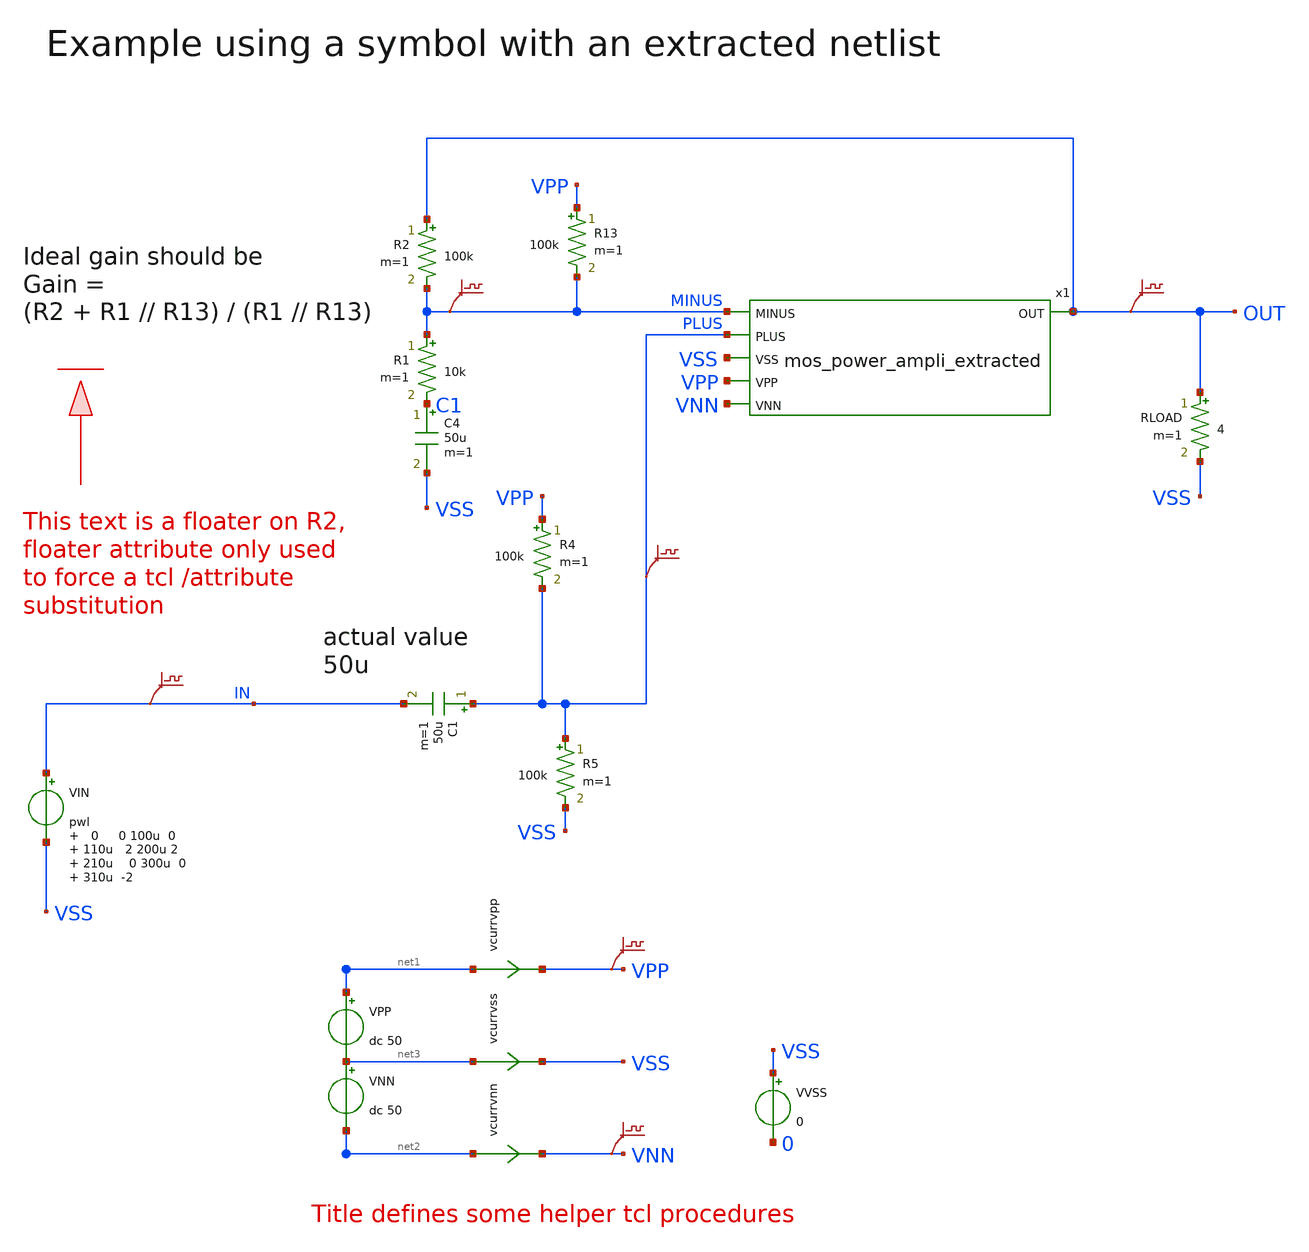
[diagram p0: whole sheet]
** sch_path: xschem-src/xschem_library/examples/test_extracted_netlist.sch
* Copyright (C) 1998-2026 Stefan Frederik Schippers
* This program is free software; you can redistribute it and/or modify
* it under the terms of the GNU General Public License as published by
* the Free Software Foundation; either version 2 of the License, or
* (at your option) any later version.
* This program is distributed in the hope that it will be useful,
* but WITHOUT ANY WARRANTY; without even the implied warranty of
* MERCHANTABILITY or FITNESS FOR A PARTICULAR PURPOSE.  See the
* GNU General Public License for more details.
* You should have received a copy of the GNU General Public License
* along with this program; if not, write to the Free Software
**.subckt test_extracted_netlist
R1 MINUS C1 10k m=1
R2 OUT MINUS 100k m=1
VPP net1 net3 dc 50
VNN net3 net2 dc 50
vcurrvpp net1 VPP 0
.save i(vcurrvpp)
vcurrvnn net2 VNN 0
.save i(vcurrvnn)
vcurrvss net3 VSS 0
.save i(vcurrvss)
.save v(vpp)
.save v(vnn)
VVSS VSS 0 0
VIN IN VSS pwl 0 0 100u 0 110u 2 200u 2 210u 0 300u 0 310u -2
.save v(out)
.save v(minus)
.save v(in)
R4 VPP PLUS 100k m=1
R5 PLUS VSS 100k m=1
C1 PLUS IN 50u m=1
C4 C1 VSS 50u m=1
R13 VPP MINUS 100k m=1
RLOAD OUT VSS 4 m=1
.save v(plus)
x1 MINUS PLUS VSS OUT VPP VNN mos_power_ampli_extracted
**** begin user architecture code

.include "models_poweramp.txt"
.options method=gear savecurrents ITL4=500 ITL5=50000  CHGTOL=1e-15 TRTOL=1
.control
save all
op
write test_extracted_netlist.raw
set appendwrite
tran  100n 400u
* .FOUR 20k v(outm,outp)
* .probe i(*)
write test_extracted_netlist.raw
.endc


**** end user architecture code
**.ends

* expanding   symbol:  mos_power_ampli_extracted.sym # of pins=6
** sym_path: xschem-src/xschem_library/examples/mos_power_ampli_extracted.sym
** sch_path: xschem-src/xschem_library/examples/mos_power_ampli_extracted.sch
.subckt mos_power_ampli_extracted MINUS PLUS VSS OUT VPP VNN
*.ipin PLUS
*.ipin VPP
*.ipin VNN
*.opin OUT
*.ipin MINUS
*.ipin VSS
* noconn MINUS
* noconn PLUS
* noconn VSS
* noconn VPP
* noconn VNN
* noconn OUT
**** begin user architecture code
xm2 net1 GB SB irf540 m=1
R7 GB SB 190 m=1
xm1 VPP GA SA irf540 m=1
R0 GA SA 190 m=1
R2 VPP E2 50 m=1
R3 VBOOST E1 50 m=1
Q5 C5 PLUS E9 q2n2222 area=1 m=1
Q4 net8 net2 E4 q2n2907p area=1 m=1
R9 VBOOST E4 50 m=1
Q6 C6 C2 net5 q2n2907p area=1 m=1
R4 VPP E6 50 m=1
vd OUTI net1 0
.save  i(vd)
vu SA OUTI 0
.save  i(vu)
Q1 net2 net2 E1 q2n2907p area=1 m=1
Q2 C2 C2 net4 q2n2907p area=1 m=1
Q9 C9 MINUS E9 q2n2222 area=1 m=1
R11 GB net6 1300 m=1
Q8 C8 VSS E8 q2n2907p area=1 m=1
C12 VBOOST net3 40u m=1
D0 VPP VBOOST d1n4148 area=1
R18 net3 OUTI 200 m=1
D1 VPP VBOOST d1n758
R14 B1 net7 4k m=1
Q11 GA B1 E11 q2n2907p area=1 m=1
R15 VBOOST B1 4k m=1
R5 E9 net9 120 m=1
R6 net9 net10 120 m=1
D2 VSS B3 d1n755
Q3 C3 B3 E3 q2n2222 area=1 m=1
R1 VPP B3 10k m=1
R10 E3 VSS 170 m=1
C3 B3 VSS 100n m=1
R12 C6 E8 1300 m=1
R13 C2 C9 300 m=1
Q7 C7 C9 C5 q2n2222 area=1 m=1
v0 SB VNN 0
.save  i(v0)
v1 E6 net5 0
.save  i(v1)
v2 E2 net4 0
.save  i(v2)
v3 net10 C3 0
.save  i(v3)
v4 C8 net6 0
.save  i(v4)
v5 net7 OUTI 0
.save  i(v5)
v6 net2 C7 0
.save  i(v6)
v7 net8 E11 0
.save  i(v7)
.save  v(gb)
.save  v(sb)
.save  v(ga)
.save  v(sa)
v8 OUTI OUT 0
.save  i(v8)
.save  v(ga)
.save  v(gb)
.save  v(c2)
.save  v(net2)
.save  v(c7)
.save  v(vboost)
.save  v(outi)
**** end user architecture code
.ends

.end
